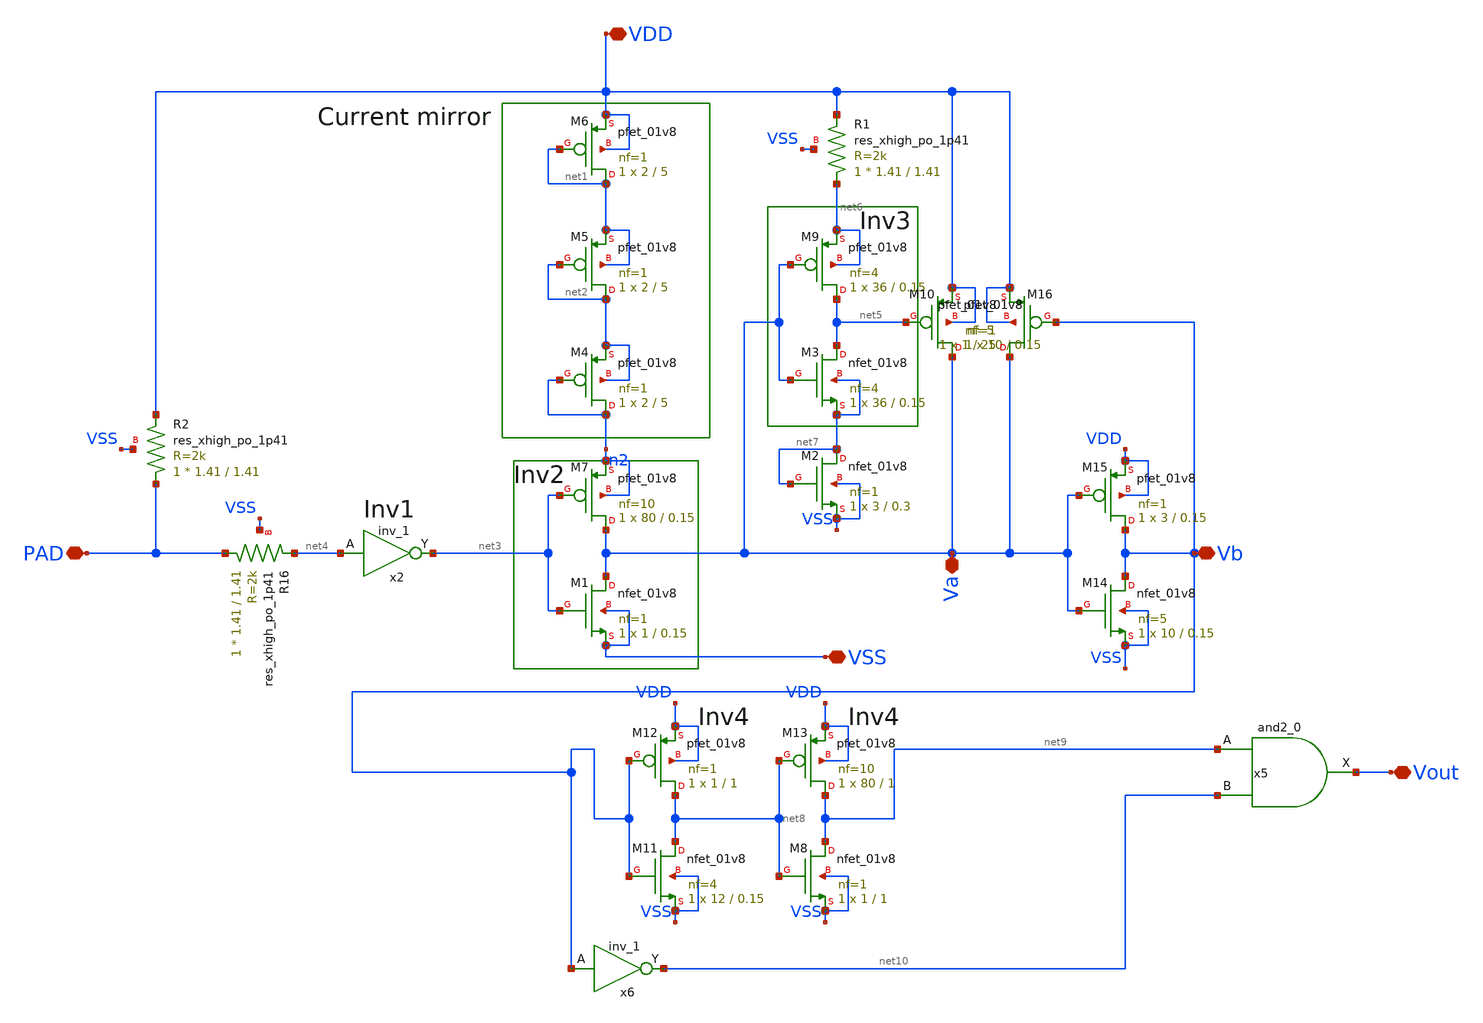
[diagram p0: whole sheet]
** sch_path: xschem/por.sch
**.subckt por Vout Vb Va VDD VSS PAD
*.iopin Vout
*.iopin Vb
*.iopin Va
*.iopin VDD
*.iopin VSS
*.iopin PAD
XM1 Va net3 VSS VSS sky130_fd_pr__nfet_01v8 L=0.15 W=1 nf=1 ad='int((nf+1)/2) * W/nf * 0.29' as='int((nf+2)/2) * W/nf * 0.29'
+ pd='2*int((nf+1)/2) * (W/nf + 0.29)' ps='2*int((nf+2)/2) * (W/nf + 0.29)' nrd='0.29 / W' nrs='0.29 / W'
+ sa=0 sb=0 sd=0 mult=1 m=1
XM2 net7 net7 VSS VSS sky130_fd_pr__nfet_01v8 L=0.3 W=3 nf=1 ad='int((nf+1)/2) * W/nf * 0.29' as='int((nf+2)/2) * W/nf * 0.29'
+ pd='2*int((nf+1)/2) * (W/nf + 0.29)' ps='2*int((nf+2)/2) * (W/nf + 0.29)' nrd='0.29 / W' nrs='0.29 / W'
+ sa=0 sb=0 sd=0 mult=1 m=1
XM3 net5 Va net7 net7 sky130_fd_pr__nfet_01v8 L=0.15 W=36 nf=4 ad='int((nf+1)/2) * W/nf * 0.29' as='int((nf+2)/2) * W/nf * 0.29'
+ pd='2*int((nf+1)/2) * (W/nf + 0.29)' ps='2*int((nf+2)/2) * (W/nf + 0.29)' nrd='0.29 / W' nrs='0.29 / W'
+ sa=0 sb=0 sd=0 mult=1 m=1
XM4 n2 n2 net2 net2 sky130_fd_pr__pfet_01v8 L=5 W=2 nf=1 ad='int((nf+1)/2) * W/nf * 0.29' as='int((nf+2)/2) * W/nf * 0.29'
+ pd='2*int((nf+1)/2) * (W/nf + 0.29)' ps='2*int((nf+2)/2) * (W/nf + 0.29)' nrd='0.29 / W' nrs='0.29 / W'
+ sa=0 sb=0 sd=0 mult=1 m=1
XM5 net2 net2 net1 net1 sky130_fd_pr__pfet_01v8 L=5 W=2 nf=1 ad='int((nf+1)/2) * W/nf * 0.29' as='int((nf+2)/2) * W/nf * 0.29'
+ pd='2*int((nf+1)/2) * (W/nf + 0.29)' ps='2*int((nf+2)/2) * (W/nf + 0.29)' nrd='0.29 / W' nrs='0.29 / W'
+ sa=0 sb=0 sd=0 mult=1 m=1
XM6 net1 net1 VDD VDD sky130_fd_pr__pfet_01v8 L=5 W=2 nf=1 ad='int((nf+1)/2) * W/nf * 0.29' as='int((nf+2)/2) * W/nf * 0.29'
+ pd='2*int((nf+1)/2) * (W/nf + 0.29)' ps='2*int((nf+2)/2) * (W/nf + 0.29)' nrd='0.29 / W' nrs='0.29 / W'
+ sa=0 sb=0 sd=0 mult=1 m=1
XM7 Va net3 n2 n2 sky130_fd_pr__pfet_01v8 L=0.15 W=80 nf=10 ad='int((nf+1)/2) * W/nf * 0.29' as='int((nf+2)/2) * W/nf * 0.29'
+ pd='2*int((nf+1)/2) * (W/nf + 0.29)' ps='2*int((nf+2)/2) * (W/nf + 0.29)' nrd='0.29 / W' nrs='0.29 / W'
+ sa=0 sb=0 sd=0 mult=1 m=1
XM9 net5 Va net6 net6 sky130_fd_pr__pfet_01v8 L=0.15 W=36 nf=4 ad='int((nf+1)/2) * W/nf * 0.29' as='int((nf+2)/2) * W/nf * 0.29'
+ pd='2*int((nf+1)/2) * (W/nf + 0.29)' ps='2*int((nf+2)/2) * (W/nf + 0.29)' nrd='0.29 / W' nrs='0.29 / W'
+ sa=0 sb=0 sd=0 mult=1 m=1
XM10 Va net5 VDD VDD sky130_fd_pr__pfet_01v8 L=0.15 W=10 nf=5 ad='int((nf+1)/2) * W/nf * 0.29' as='int((nf+2)/2) * W/nf * 0.29'
+ pd='2*int((nf+1)/2) * (W/nf + 0.29)' ps='2*int((nf+2)/2) * (W/nf + 0.29)' nrd='0.29 / W' nrs='0.29 / W'
+ sa=0 sb=0 sd=0 mult=1 m=1
x2 net4 VSS VSS VDD VDD net3 sky130_fd_sc_hd__inv_1
x5 net9 net10 VSS VSS VDD VDD Vout sky130_fd_sc_hd__and2_0
XM11 net8 Vb VSS VSS sky130_fd_pr__nfet_01v8 L=0.15 W=12 nf=4 ad='int((nf+1)/2) * W/nf * 0.29' as='int((nf+2)/2) * W/nf * 0.29'
+ pd='2*int((nf+1)/2) * (W/nf + 0.29)' ps='2*int((nf+2)/2) * (W/nf + 0.29)' nrd='0.29 / W' nrs='0.29 / W'
+ sa=0 sb=0 sd=0 mult=1 m=1
XM12 net8 Vb VDD VDD sky130_fd_pr__pfet_01v8 L=1 W=1 nf=1 ad='int((nf+1)/2) * W/nf * 0.29' as='int((nf+2)/2) * W/nf * 0.29'
+ pd='2*int((nf+1)/2) * (W/nf + 0.29)' ps='2*int((nf+2)/2) * (W/nf + 0.29)' nrd='0.29 / W' nrs='0.29 / W'
+ sa=0 sb=0 sd=0 mult=1 m=1
x6 Vb VSS VSS VDD VDD net10 sky130_fd_sc_hd__inv_1
XM8 net9 net8 VSS VSS sky130_fd_pr__nfet_01v8 L=1 W=1 nf=1 ad='int((nf+1)/2) * W/nf * 0.29' as='int((nf+2)/2) * W/nf * 0.29'
+ pd='2*int((nf+1)/2) * (W/nf + 0.29)' ps='2*int((nf+2)/2) * (W/nf + 0.29)' nrd='0.29 / W' nrs='0.29 / W'
+ sa=0 sb=0 sd=0 mult=1 m=1
XM13 net9 net8 VDD VDD sky130_fd_pr__pfet_01v8 L=1 W=80 nf=10 ad='int((nf+1)/2) * W/nf * 0.29' as='int((nf+2)/2) * W/nf * 0.29'
+ pd='2*int((nf+1)/2) * (W/nf + 0.29)' ps='2*int((nf+2)/2) * (W/nf + 0.29)' nrd='0.29 / W' nrs='0.29 / W'
+ sa=0 sb=0 sd=0 mult=1 m=1
XM14 Vb Va VSS VSS sky130_fd_pr__nfet_01v8 L=0.15 W=10 nf=5 ad='int((nf+1)/2) * W/nf * 0.29' as='int((nf+2)/2) * W/nf * 0.29'
+ pd='2*int((nf+1)/2) * (W/nf + 0.29)' ps='2*int((nf+2)/2) * (W/nf + 0.29)' nrd='0.29 / W' nrs='0.29 / W'
+ sa=0 sb=0 sd=0 mult=1 m=1
XM15 Vb Va VDD VDD sky130_fd_pr__pfet_01v8 L=0.15 W=3 nf=1 ad='int((nf+1)/2) * W/nf * 0.29' as='int((nf+2)/2) * W/nf * 0.29'
+ pd='2*int((nf+1)/2) * (W/nf + 0.29)' ps='2*int((nf+2)/2) * (W/nf + 0.29)' nrd='0.29 / W' nrs='0.29 / W'
+ sa=0 sb=0 sd=0 mult=1 m=1
XM16 Va Vb VDD VDD sky130_fd_pr__pfet_01v8 L=25 W=1 nf=1 ad='int((nf+1)/2) * W/nf * 0.29' as='int((nf+2)/2) * W/nf * 0.29'
+ pd='2*int((nf+1)/2) * (W/nf + 0.29)' ps='2*int((nf+2)/2) * (W/nf + 0.29)' nrd='0.29 / W' nrs='0.29 / W'
+ sa=0 sb=0 sd=0 mult=1 m=1
XR16 PAD net4 VSS sky130_fd_pr__res_xhigh_po_1p41 L=1.41 mult=1 m=1
XR1 net6 VDD VSS sky130_fd_pr__res_xhigh_po_1p41 L=1.41 mult=1 m=1
XR2 PAD VDD VSS sky130_fd_pr__res_xhigh_po_1p41 L=1.41 mult=1 m=1
**.ends
.end
